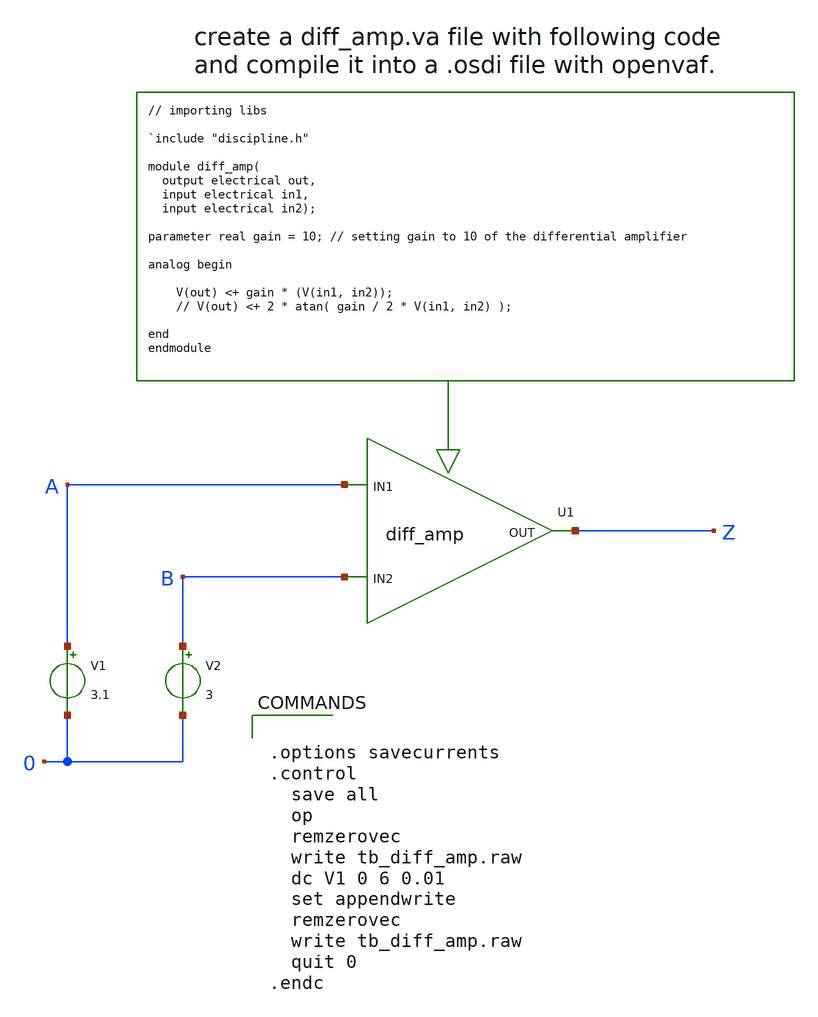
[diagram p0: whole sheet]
** sch_path: sky130_tests/tb_diff_amp.sch
* StefanSchippers/xschem/xschem_library/ngspice/diff_amp.sym:
* Copyright (C) 1998-2024 Stefan Frederik Schippers
* This program is free software; you can redistribute it and/or modify
* it under the terms of the GNU General Public License as published by
* the Free Software Foundation; either version 2 of the License, or
* (at your option) any later version.
**.subckt tb_diff_amp
U1 Z A B diff_amp_cell gain=40 amplitude=3 offset=1.5
V1 A 0 3.1
V2 B 0 3
**** begin user architecture code


.options savecurrents
.control
  save all
  op
  remzerovec
  write tb_diff_amp.raw
  dc V1 0 6 0.01
  set appendwrite
  remzerovec
  write tb_diff_amp.raw
  quit 0
.endc


**** end user architecture code
**.ends
**** begin user architecture code

.control
* following line specifies the location for the .osdi file so ngspice can use it.
pre_osdi [abs_sym_path diff_amp.osdi]
.endc

.model diff_amp_model diff_amp $ gain=40 amplitude=3 offset=1.5

.subckt diff_amp_cell OUT IN1 IN2 gain=40 amplitude=3 offset=1.5
N1 out in1 in2 diff_amp_model gain=gain amplitude=amplitude offset=offset
.ends diff_amp_cell

**** end user architecture code
.end
